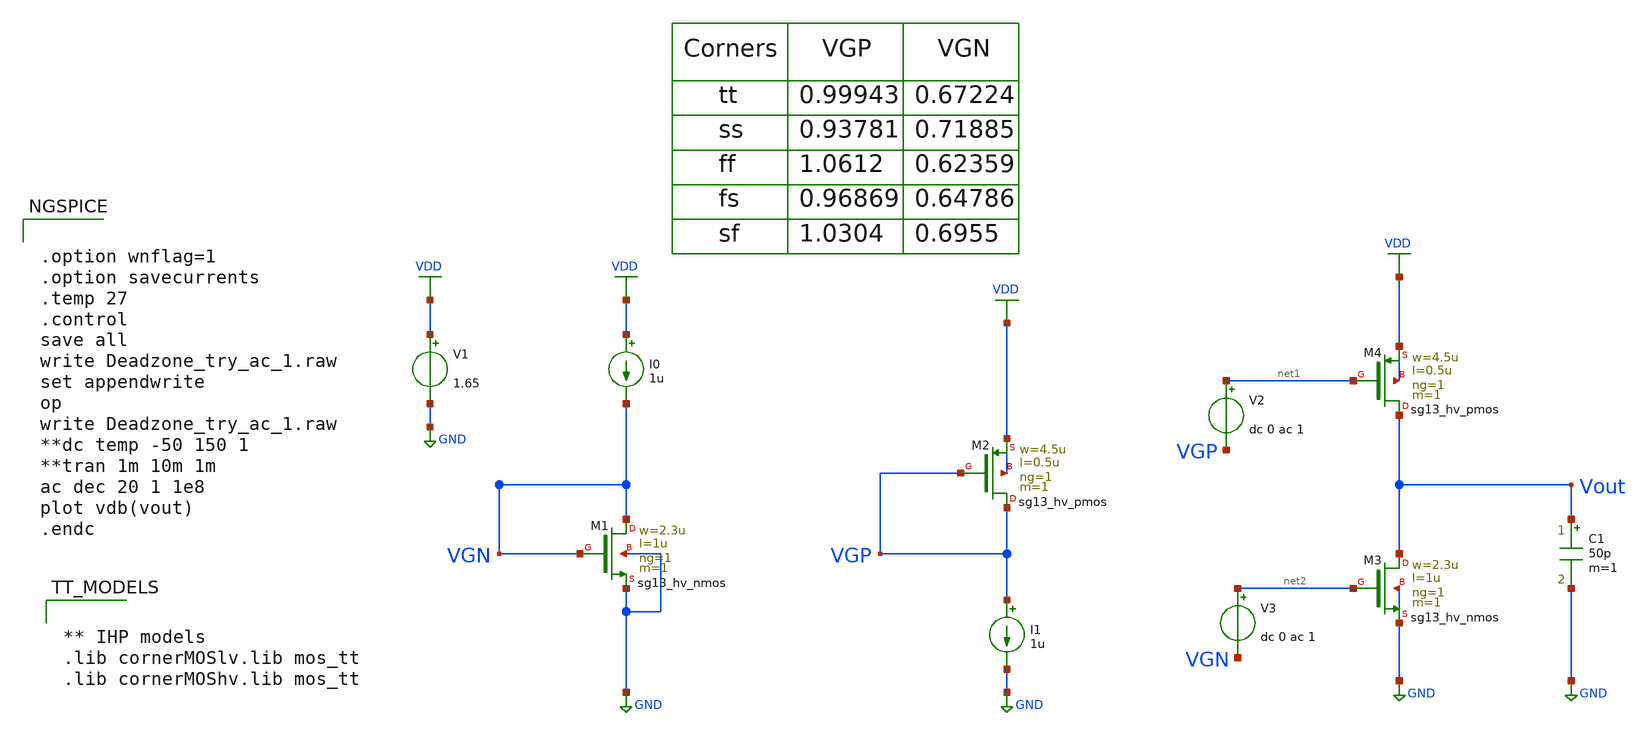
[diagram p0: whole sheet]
** sch_path: Design Files/RAMP/STG3/Deadzone_try_ac_1.sch
**.subckt Deadzone_try_ac_1
I0 VDD VGN 1u
I1 VGP GND 1u
V1 VDD GND 1.65
V2 net1 VGP dc 0 ac 1
V3 net2 VGN dc 0 ac 1
C1 Vout GND 50p m=1
XM1 VGN VGN GND GND sg13_hv_nmos w=2.3u l=1u ng=1 m=1 mm_ok=1
XM2 VGP VGP VDD VDD sg13_hv_pmos w=4.5u l=0.5u ng=1 m=1 mm_ok=1
XM4 Vout net1 VDD VDD sg13_hv_pmos w=4.5u l=0.5u ng=1 m=1 mm_ok=1
XM3 Vout net2 GND GND sg13_hv_nmos w=2.3u l=1u ng=1 m=1 mm_ok=1
**** begin user architecture code


.option wnflag=1
.option savecurrents
.temp 27
.control
save all
write Deadzone_try_ac_1.raw
set appendwrite
op
write Deadzone_try_ac_1.raw
**dc temp -50 150 1
**tran 1m 10m 1m
ac dec 20 1 1e8
plot vdb(vout)
.endc




** IHP models
.lib cornerMOSlv.lib mos_tt
.lib cornerMOShv.lib mos_tt




.save @n.xm1.nsg13_hv_nmos[gds]
.save @n.xm1.nsg13_hv_nmos[gm]
.save @n.xm1.nsg13_hv_nmos[gmb]
.save @n.xm1.nsg13_hv_nmos[ids]
.save @n.xm1.nsg13_hv_nmos[l]
.save @n.xm1.nsg13_hv_nmos[vth]
.save @n.xm1.nsg13_hv_nmos[vgs]
.save @n.xm1.nsg13_hv_nmos[vds]
.save @n.xm1.nsg13_hv_nmos[cgg]
.save @n.xm1.nsg13_hv_nmos[vsat]
.save @n.xm2.nsg13_hv_pmos[cgd]
.save @n.xm2.nsg13_hv_pmos[cgg]
.save @n.xm2.nsg13_hv_pmos[cgs]
.save @n.xm2.nsg13_hv_pmos[gds]
.save @n.xm2.nsg13_hv_pmos[gm]
.save @n.xm2.nsg13_hv_pmos[gmb]
.save @n.xm2.nsg13_hv_pmos[ids]
.save @n.xm2.nsg13_hv_pmos[l]
.save @n.xm2.nsg13_hv_pmos[vsat]
.save @n.xm2.nsg13_hv_pmos[vth]
.save @n.xm2.nsg13_hv_pmos[vgs]
.save @n.xm2.nsg13_hv_pmos[vds]
.save @n.xm4.nsg13_hv_pmos[cgd]
.save @n.xm4.nsg13_hv_pmos[vsat]
.save @n.xm4.nsg13_hv_pmos[cgg]
.save @n.xm4.nsg13_hv_pmos[cgs]
.save @n.xm4.nsg13_hv_pmos[gds]
.save @n.xm4.nsg13_hv_pmos[gm]
.save @n.xm4.nsg13_hv_pmos[gmb]
.save @n.xm4.nsg13_hv_pmos[ids]
.save @n.xm4.nsg13_hv_pmos[l]
.save @n.xm4.nsg13_hv_pmos[vth]
.save @n.xm4.nsg13_hv_pmos[vgs]
.save @n.xm4.nsg13_hv_pmos[vds]
.save @n.xm3.nsg13_hv_nmos[gds]
.save @n.xm3.nsg13_hv_nmos[gm]
.save @n.xm3.nsg13_hv_nmos[gmb]
.save @n.xm3.nsg13_hv_nmos[ids]
.save @n.xm3.nsg13_hv_nmos[l]
.save @n.xm3.nsg13_hv_nmos[vth]
.save @n.xm3.nsg13_hv_nmos[vgs]
.save @n.xm3.nsg13_hv_nmos[vds]
.save @n.xm3.nsg13_hv_nmos[cgg]
.save @n.xm3.nsg13_hv_nmos[vsat]


**** end user architecture code
**.ends
.GLOBAL VDD
.GLOBAL GND
.end
